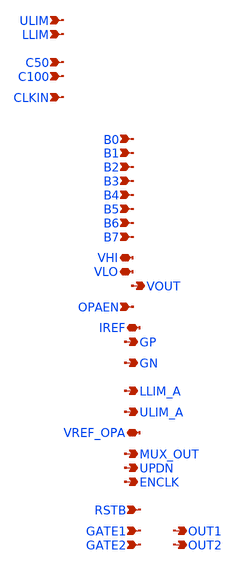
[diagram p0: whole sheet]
** sch_path: xschem/twg_PEX.sch
**.subckt twg_PEX ULIM C50 C100 CLKIN LLIM VHI VLO B0 B1 B2 B3 B4 B5 B6 B7 VOUT OPAEN IREF GP GN
*+ LLIM_A ULIM_A VREF_OPA MUX_OUT UPDN ENCLK RSTB GATE1 GATE2 OUT1 OUT2
*.ipin ULIM
*.ipin C50
*.ipin C100
*.ipin CLKIN
*.ipin LLIM
*.iopin VHI
*.iopin VLO
*.ipin B0
*.ipin B1
*.ipin B2
*.ipin B3
*.ipin B4
*.ipin B5
*.ipin B6
*.ipin B7
*.opin VOUT
*.ipin OPAEN
*.iopin IREF
*.opin GP
*.opin GN
*.opin LLIM_A
*.opin ULIM_A
*.iopin VREF_OPA
*.opin MUX_OUT
*.opin UPDN
*.opin ENCLK
*.ipin RSTB
*.ipin GATE1
*.ipin GATE2
*.opin OUT1
*.opin OUT2
**** begin user architecture code

* NGSPICE file created from twg_top_test.ext - technology: sky130A

.subckt sky130_fd_sc_hs__diode_2 DIODE VGND VPB VPWR VNB
D0 VNB DIODE sky130_fd_pr__diode_pw2nd_05v5 pj=3.24e+06 area=6.417e+11
.ends

.subckt sky130_fd_sc_hs__decap_8 VGND VPWR VNB VPB
X0 VPWR VGND VPWR VPB sky130_fd_pr__pfet_01v8 ad=8.35e+11p pd=7.67e+06u as=0p ps=0u w=1e+06u
+ l=1e+06u
X1 VPWR VGND VPWR VPB sky130_fd_pr__pfet_01v8 ad=0p pd=0u as=0p ps=0u w=1e+06u l=1e+06u
X2 VGND VPWR VGND VNB sky130_fd_pr__nfet_01v8_lvt ad=3.465e+11p pd=4.17e+06u as=0p ps=0u w=420000u
+ l=1e+06u
X3 VGND VPWR VGND VNB sky130_fd_pr__nfet_01v8_lvt ad=0p pd=0u as=0p ps=0u w=420000u l=1e+06u
.ends

.subckt tcap_50f C S VLO
X0 a_173_157# C sky130_fd_pr__cap_mim_m3_2 l=1.6e+06u w=7.85e+06u
X1 a_173_157# S VLO VLO sky130_fd_pr__nfet_01v8 ad=5.8e+11p pd=4.58e+06u as=5.8e+11p ps=4.58e+06u
+ w=2e+06u l=150000u
X2 C a_173_157# sky130_fd_pr__cap_mim_m3_1 l=1.6e+06u w=7.85e+06u
.ends

.subckt sky130_fd_sc_hs__mux2_1 A0 A1 S VGND VPWR X VNB VPB
X0 VGND a_27_112# a_443_74# VNB sky130_fd_pr__nfet_01v8_lvt ad=7.0725e+11p pd=4.91e+06u
+ as=5.994e+11p ps=3.1e+06u w=740000u l=150000u
X1 VPWR S a_27_112# VPB sky130_fd_pr__pfet_01v8 ad=8.82e+11p pd=5.95e+06u as=2.478e+11p ps=2.27e+06u
+ w=840000u l=150000u
X2 X a_304_74# VPWR VPB sky130_fd_pr__pfet_01v8 ad=3.304e+11p pd=2.83e+06u as=0p ps=0u w=1.12e+06u
+ l=150000u
X3 VPWR a_27_112# a_524_368# VPB sky130_fd_pr__pfet_01v8 ad=0p pd=0u as=4.2e+11p ps=2.84e+06u
+ w=1e+06u l=150000u
X4 a_304_74# A1 a_226_74# VNB sky130_fd_pr__nfet_01v8_lvt ad=4.033e+11p pd=2.57e+06u as=1.776e+11p
+ ps=1.96e+06u w=740000u l=150000u
X5 X a_304_74# VGND VNB sky130_fd_pr__nfet_01v8_lvt ad=2.109e+11p pd=2.05e+06u as=0p ps=0u w=740000u
+ l=150000u
X6 a_223_368# S VPWR VPB sky130_fd_pr__pfet_01v8 ad=8.15e+11p pd=3.63e+06u as=0p ps=0u w=1e+06u
+ l=150000u
X7 a_304_74# A0 a_223_368# VPB sky130_fd_pr__pfet_01v8 ad=3.9e+11p pd=2.78e+06u as=0p ps=0u w=1e+06u
+ l=150000u
X8 a_443_74# A0 a_304_74# VNB sky130_fd_pr__nfet_01v8_lvt ad=0p pd=0u as=0p ps=0u w=740000u
+ l=150000u
X9 a_524_368# A1 a_304_74# VPB sky130_fd_pr__pfet_01v8 ad=0p pd=0u as=0p ps=0u w=1e+06u l=150000u
X10 a_226_74# S VGND VNB sky130_fd_pr__nfet_01v8_lvt ad=0p pd=0u as=0p ps=0u w=740000u l=150000u
X11 VGND S a_27_112# VNB sky130_fd_pr__nfet_01v8_lvt ad=0p pd=0u as=1.5675e+11p ps=1.67e+06u
+ w=550000u l=150000u
.ends

.subckt sky130_fd_sc_hs__decap_4 VGND VPWR VNB VPB
X0 VPWR VGND VPWR VPB sky130_fd_pr__pfet_01v8 ad=5.6e+11p pd=5.12e+06u as=0p ps=0u w=1e+06u l=1e+06u
X1 VGND VPWR VGND VNB sky130_fd_pr__nfet_01v8_lvt ad=2.31e+11p pd=2.78e+06u as=0p ps=0u w=420000u
+ l=1e+06u
.ends

.subckt tcap_100f C S VLO
X0 a_173_157# C sky130_fd_pr__cap_mim_m3_2 l=1.6e+06u w=1.57e+07u
X1 a_173_157# S VLO VLO sky130_fd_pr__nfet_01v8 ad=5.8e+11p pd=4.58e+06u as=5.8e+11p ps=4.58e+06u
+ w=2e+06u l=150000u
X2 C a_173_157# sky130_fd_pr__cap_mim_m3_1 l=1.6e+06u w=1.57e+07u
.ends

.subckt sky130_fd_sc_hs__sdfbbn_2 CLK_N D RESET_B SCD SCE SET_B VGND VPWR Q Q_N VNB  VPB
X0 a_1997_82# a_868_368# a_1986_424# VPB sky130_fd_pr__pfet_01v8 ad=2.856e+11p pd=2.45e+06u
+ as=2.016e+11p ps=2.16e+06u w=840000u l=150000u
X1 a_1185_125# a_1007_366# VGND VNB sky130_fd_pr__nfet_01v8_lvt ad=8.82e+10p pd=1.26e+06u
+ as=2.86405e+12p ps=2.37e+07u w=420000u l=150000u
X2 a_2452_74# SET_B VGND VNB sky130_fd_pr__nfet_01v8_lvt ad=5.7435e+11p pd=4.64e+06u as=0p ps=0u
+ w=740000u l=150000u
X3 a_1070_464# a_1007_366# VPWR VPB sky130_fd_pr__pfet_01v8 ad=1.134e+11p pd=1.38e+06u
+ as=4.12873e+12p ps=3.022e+07u w=420000u l=150000u
X4 a_363_119# D a_197_119# VNB sky130_fd_pr__nfet_01v8_lvt ad=1.008e+11p pd=1.32e+06u as=4.347e+11p
+ ps=3.75e+06u w=420000u l=150000u
X5 VGND a_2216_410# Q_N VNB sky130_fd_pr__nfet_01v8_lvt ad=0p pd=0u as=2.072e+11p ps=2.04e+06u
+ w=740000u l=150000u
X6 VGND a_2216_410# a_3272_94# VNB sky130_fd_pr__nfet_01v8_lvt ad=0p pd=0u as=1.824e+11p
+ ps=1.85e+06u w=640000u l=150000u
X7 a_119_119# SCD VGND VNB sky130_fd_pr__nfet_01v8_lvt ad=1.008e+11p pd=1.32e+06u as=0p ps=0u
+ w=420000u l=150000u
X8 VGND SET_B a_1473_73# VNB sky130_fd_pr__nfet_01v8_lvt ad=0p pd=0u as=6.0335e+11p ps=4.55e+06u
+ w=550000u l=150000u
X9 a_2247_82# a_868_368# a_1997_82# VNB sky130_fd_pr__nfet_01v8_lvt ad=1.008e+11p pd=1.32e+06u
+ as=4.945e+11p ps=3.3e+06u w=420000u l=150000u
X10 VGND CLK_N a_688_98# VNB sky130_fd_pr__nfet_01v8_lvt ad=0p pd=0u as=2.109e+11p ps=2.05e+06u
+ w=740000u l=150000u
X11 a_868_368# a_688_98# VGND VNB sky130_fd_pr__nfet_01v8_lvt ad=2.109e+11p pd=2.05e+06u as=0p ps=0u
+ w=740000u l=150000u
X12 VPWR a_3272_94# Q VPB sky130_fd_pr__pfet_01v8 ad=0p pd=0u as=3.36e+11p ps=2.84e+06u w=1.12e+06u
+ l=150000u
X13 a_2452_74# a_1997_82# a_2216_410# VNB sky130_fd_pr__nfet_01v8_lvt ad=0p pd=0u as=2.072e+11p
+ ps=2.04e+06u w=740000u l=150000u
X14 VPWR SCD a_27_464# VPB sky130_fd_pr__pfet_01v8 ad=0p pd=0u as=3.776e+11p ps=3.74e+06u w=640000u
+ l=150000u
X15 Q a_3272_94# VPWR VPB sky130_fd_pr__pfet_01v8 ad=0p pd=0u as=0p ps=0u w=1.12e+06u l=150000u
X16 a_1986_424# a_1007_366# VPWR VPB sky130_fd_pr__pfet_01v8 ad=0p pd=0u as=0p ps=0u w=840000u
+ l=150000u
X17 VPWR a_2216_410# a_2171_508# VPB sky130_fd_pr__pfet_01v8 ad=0p pd=0u as=1.008e+11p ps=1.32e+06u
+ w=420000u l=150000u
X18 a_2216_410# a_1997_82# a_2556_392# VPB sky130_fd_pr__pfet_01v8 ad=5.9e+11p pd=5.18e+06u
+ as=2.7e+11p ps=2.54e+06u w=1e+06u l=150000u
X19 a_341_410# SCE VPWR VPB sky130_fd_pr__pfet_01v8 ad=1.888e+11p pd=1.87e+06u as=0p ps=0u w=640000u
+ l=150000u
X20 a_1007_366# a_1154_464# a_1473_73# VNB sky130_fd_pr__nfet_01v8_lvt ad=1.54e+11p pd=1.66e+06u
+ as=0p ps=0u w=550000u l=150000u
X21 VPWR SET_B a_2216_410# VPB sky130_fd_pr__pfet_01v8 ad=0p pd=0u as=0p ps=0u w=1e+06u l=150000u
X22 VGND a_3272_94# Q VNB sky130_fd_pr__nfet_01v8_lvt ad=0p pd=0u as=2.072e+11p ps=2.04e+06u
+ w=740000u l=150000u
X23 VPWR a_1643_257# a_1592_424# VPB sky130_fd_pr__pfet_01v8 ad=0p pd=0u as=2.268e+11p ps=2.22e+06u
+ w=840000u l=150000u
X24 a_2171_508# a_688_98# a_1997_82# VPB sky130_fd_pr__pfet_01v8 ad=0p pd=0u as=0p ps=0u w=420000u
+ l=150000u
X25 a_1997_82# a_688_98# a_1902_125# VNB sky130_fd_pr__nfet_01v8_lvt ad=0p pd=0u as=2.16375e+11p
+ ps=2.18e+06u w=550000u l=150000u
X26 a_2556_392# a_1643_257# VPWR VPB sky130_fd_pr__pfet_01v8 ad=0p pd=0u as=0p ps=0u w=1e+06u
+ l=150000u
X27 a_1592_424# a_1154_464# a_1007_366# VPB sky130_fd_pr__pfet_01v8 ad=0p pd=0u as=9.954e+11p
+ ps=5.73e+06u w=840000u l=150000u
X28 a_1007_366# SET_B VPWR VPB sky130_fd_pr__pfet_01v8 ad=0p pd=0u as=0p ps=0u w=840000u l=150000u
X29 VPWR RESET_B a_1643_257# VPB sky130_fd_pr__pfet_01v8 ad=0p pd=0u as=1.888e+11p ps=1.87e+06u
+ w=640000u l=150000u
X30 VPWR a_2216_410# Q_N VPB sky130_fd_pr__pfet_01v8 ad=0p pd=0u as=3.36e+11p ps=2.84e+06u
+ w=1.12e+06u l=150000u
X31 a_2216_410# a_1643_257# a_2452_74# VNB sky130_fd_pr__nfet_01v8_lvt ad=0p pd=0u as=0p ps=0u
+ w=740000u l=150000u
X32 a_197_119# SCE a_119_119# VNB sky130_fd_pr__nfet_01v8_lvt ad=0p pd=0u as=0p ps=0u w=420000u
+ l=150000u
X33 Q_N a_2216_410# VPWR VPB sky130_fd_pr__pfet_01v8 ad=0p pd=0u as=0p ps=0u w=1.12e+06u l=150000u
X34 VGND a_2216_410# a_2247_82# VNB sky130_fd_pr__nfet_01v8_lvt ad=0p pd=0u as=0p ps=0u w=420000u
+ l=150000u
X35 a_27_464# a_341_410# a_197_119# VPB sky130_fd_pr__pfet_01v8 ad=0p pd=0u as=4.128e+11p
+ ps=3.85e+06u w=640000u l=150000u
X36 a_1473_73# a_1643_257# a_1007_366# VNB sky130_fd_pr__nfet_01v8_lvt ad=0p pd=0u as=0p ps=0u
+ w=550000u l=150000u
X37 a_197_119# D a_206_464# VPB sky130_fd_pr__pfet_01v8 ad=0p pd=0u as=1.536e+11p ps=1.76e+06u
+ w=640000u l=150000u
X38 a_1154_464# a_688_98# a_1185_125# VNB sky130_fd_pr__nfet_01v8_lvt ad=1.281e+11p pd=1.45e+06u
+ as=0p ps=0u w=420000u l=150000u
X39 a_1902_125# a_1007_366# VGND VNB sky130_fd_pr__nfet_01v8_lvt ad=0p pd=0u as=0p ps=0u w=550000u
+ l=150000u
X40 Q a_3272_94# VGND VNB sky130_fd_pr__nfet_01v8_lvt ad=0p pd=0u as=0p ps=0u w=740000u l=150000u
X41 a_197_119# a_688_98# a_1154_464# VPB sky130_fd_pr__pfet_01v8 ad=0p pd=0u as=2.266e+11p
+ ps=2.05e+06u w=640000u l=150000u
X42 VPWR a_2216_410# a_3272_94# VPB sky130_fd_pr__pfet_01v8 ad=0p pd=0u as=2.9e+11p ps=2.58e+06u
+ w=1e+06u l=150000u
X43 VGND RESET_B a_1643_257# VNB sky130_fd_pr__nfet_01v8_lvt ad=0p pd=0u as=1.176e+11p ps=1.4e+06u
+ w=420000u l=150000u
X44 a_868_368# a_688_98# VPWR VPB sky130_fd_pr__pfet_01v8 ad=3.304e+11p pd=2.83e+06u as=0p ps=0u
+ w=1.12e+06u l=150000u
X45 a_197_119# a_868_368# a_1154_464# VNB sky130_fd_pr__nfet_01v8_lvt ad=0p pd=0u as=0p ps=0u
+ w=420000u l=150000u
X46 a_206_464# SCE VPWR VPB sky130_fd_pr__pfet_01v8 ad=0p pd=0u as=0p ps=0u w=640000u l=150000u
X47 VPWR CLK_N a_688_98# VPB sky130_fd_pr__pfet_01v8 ad=0p pd=0u as=3.304e+11p ps=2.83e+06u
+ w=1.12e+06u l=150000u
X48 a_1154_464# a_868_368# a_1070_464# VPB sky130_fd_pr__pfet_01v8 ad=0p pd=0u as=0p ps=0u w=420000u
+ l=150000u
X49 VGND a_341_410# a_363_119# VNB sky130_fd_pr__nfet_01v8_lvt ad=0p pd=0u as=0p ps=0u w=420000u
+ l=150000u
X50 a_341_410# SCE VGND VNB sky130_fd_pr__nfet_01v8_lvt ad=1.197e+11p pd=1.41e+06u as=0p ps=0u
+ w=420000u l=150000u
X51 Q_N a_2216_410# VGND VNB sky130_fd_pr__nfet_01v8_lvt ad=0p pd=0u as=0p ps=0u w=740000u l=150000u
.ends

.subckt sky130_fd_sc_hs__inv_1 A VGND VPWR Y VNB VPB
X0 Y A VPWR VPB sky130_fd_pr__pfet_01v8 ad=3.304e+11p pd=2.83e+06u as=3.864e+11p ps=2.93e+06u
+ w=1.12e+06u l=150000u
X1 Y A VGND VNB sky130_fd_pr__nfet_01v8_lvt ad=2.109e+11p pd=2.05e+06u as=2.627e+11p ps=2.19e+06u
+ w=740000u l=150000u
.ends

.subckt sky130_fd_sc_hs__nand2_1 A B VGND VPWR Y VNB VPB
X0 a_117_74# B VGND VNB sky130_fd_pr__nfet_01v8_lvt ad=1.776e+11p pd=1.96e+06u as=2.109e+11p
+ ps=2.05e+06u w=740000u l=150000u
X1 VPWR A Y VPB sky130_fd_pr__pfet_01v8 ad=6.384e+11p pd=5.62e+06u as=3.36e+11p ps=2.84e+06u
+ w=1.12e+06u l=150000u
X2 Y A a_117_74# VNB sky130_fd_pr__nfet_01v8_lvt ad=2.109e+11p pd=2.05e+06u as=0p ps=0u w=740000u
+ l=150000u
X3 Y B VPWR VPB sky130_fd_pr__pfet_01v8 ad=0p pd=0u as=0p ps=0u w=1.12e+06u l=150000u
.ends

.subckt sky130_fd_pr__res_xhigh_po_1p41_GKKP9B a_n141_n482# a_n141_50# VSUBS
X0 a_n141_n482# a_n141_50# VSUBS sky130_fd_pr__res_xhigh_po_1p41 l=500000u
.ends

.subckt twcon_tdly C A Y sky130_fd_sc_hs__inv_1_0/VGND VSUBS sky130_fd_sc_hs__inv_1_0/VPWR
+  sky130_fd_sc_hs__inv_1_0/VPB
Xsky130_fd_sc_hs__inv_1_0 A sky130_fd_sc_hs__inv_1_0/VGND sky130_fd_sc_hs__inv_1_0/VPWR
+  sky130_fd_sc_hs__inv_1_0/Y VSUBS sky130_fd_sc_hs__inv_1_0/VPB sky130_fd_sc_hs__inv_1
Xsky130_fd_sc_hs__nand2_1_2 A C sky130_fd_sc_hs__inv_1_0/VGND sky130_fd_sc_hs__inv_1_0/VPWR  Y VSUBS
+ sky130_fd_sc_hs__inv_1_0/VPB sky130_fd_sc_hs__nand2_1
Xsky130_fd_pr__res_xhigh_po_1p41_GKKP9B_0 sky130_fd_sc_hs__inv_1_0/Y C VSUBS
+ sky130_fd_pr__res_xhigh_po_1p41_GKKP9B
.ends

.subckt sky130_fd_sc_hs__nand2_4 A B VGND VPWR Y VNB VPB
X0 Y A a_27_74# VNB sky130_fd_pr__nfet_01v8_lvt ad=5.365e+11p pd=4.41e+06u as=1.1581e+12p
+ ps=1.053e+07u w=740000u l=150000u
X1 Y B VPWR VPB sky130_fd_pr__pfet_01v8 ad=2.7496e+12p pd=9.39e+06u as=1.1144e+12p ps=8.71e+06u
+ w=1.12e+06u l=150000u
X2 VPWR A Y VPB sky130_fd_pr__pfet_01v8 ad=0p pd=0u as=0p ps=0u w=1.12e+06u l=150000u
X3 Y A a_27_74# VNB sky130_fd_pr__nfet_01v8_lvt ad=0p pd=0u as=0p ps=0u w=740000u l=150000u
X4 Y A VPWR VPB sky130_fd_pr__pfet_01v8 ad=0p pd=0u as=0p ps=0u w=1.12e+06u l=150000u
X5 VGND B a_27_74# VNB sky130_fd_pr__nfet_01v8_lvt ad=4.144e+11p pd=4.08e+06u as=0p ps=0u w=740000u
+ l=150000u
X6 a_27_74# A Y VNB sky130_fd_pr__nfet_01v8_lvt ad=0p pd=0u as=0p ps=0u w=740000u l=150000u
X7 VPWR B Y VPB sky130_fd_pr__pfet_01v8 ad=0p pd=0u as=0p ps=0u w=1.12e+06u l=150000u
X8 a_27_74# B VGND VNB sky130_fd_pr__nfet_01v8_lvt ad=0p pd=0u as=0p ps=0u w=740000u l=150000u
X9 a_27_74# A Y VNB sky130_fd_pr__nfet_01v8_lvt ad=0p pd=0u as=0p ps=0u w=740000u l=150000u
X10 a_27_74# B VGND VNB sky130_fd_pr__nfet_01v8_lvt ad=0p pd=0u as=0p ps=0u w=740000u l=150000u
X11 VGND B a_27_74# VNB sky130_fd_pr__nfet_01v8_lvt ad=0p pd=0u as=0p ps=0u w=740000u l=150000u
.ends

.subckt sky130_fd_sc_hs__inv_2 A VGND VPWR Y VNB VPB
X0 Y A VGND VNB sky130_fd_pr__nfet_01v8_lvt ad=2.072e+11p pd=2.04e+06u as=4.218e+11p ps=4.1e+06u
+ w=740000u l=150000u
X1 VPWR A Y VPB sky130_fd_pr__pfet_01v8 ad=6.384e+11p pd=5.62e+06u as=3.36e+11p ps=2.84e+06u
+ w=1.12e+06u l=150000u
X2 VGND A Y VNB sky130_fd_pr__nfet_01v8_lvt ad=0p pd=0u as=0p ps=0u w=740000u l=150000u
X3 Y A VPWR VPB sky130_fd_pr__pfet_01v8 ad=0p pd=0u as=0p ps=0u w=1.12e+06u l=150000u
.ends

.subckt sky130_fd_sc_hs__and2_4 A B VGND VPWR X VNB VPB
X0 X a_83_269# VPWR VPB sky130_fd_pr__pfet_01v8 ad=6.944e+11p pd=5.72e+06u as=1.58705e+12p
+ ps=1.328e+07u w=1.12e+06u l=150000u
X1 a_83_269# B VPWR VPB sky130_fd_pr__pfet_01v8 ad=5.25e+11p pd=4.61e+06u as=0p ps=0u w=840000u
+ l=150000u
X2 a_83_269# A a_504_119# VNB sky130_fd_pr__nfet_01v8_lvt ad=2.08e+11p pd=1.93e+06u as=3.872e+11p
+ ps=3.77e+06u w=640000u l=150000u
X3 VPWR a_83_269# X VPB sky130_fd_pr__pfet_01v8 ad=0p pd=0u as=0p ps=0u w=1.12e+06u l=150000u
X4 VGND a_83_269# X VNB sky130_fd_pr__nfet_01v8_lvt ad=8.594e+11p pd=8.14e+06u as=5.254e+11p
+ ps=4.38e+06u w=740000u l=150000u
X5 X a_83_269# VGND VNB sky130_fd_pr__nfet_01v8_lvt ad=0p pd=0u as=0p ps=0u w=740000u l=150000u
X6 X a_83_269# VPWR VPB sky130_fd_pr__pfet_01v8 ad=0p pd=0u as=0p ps=0u w=1.12e+06u l=150000u
X7 VPWR a_83_269# X VPB sky130_fd_pr__pfet_01v8 ad=0p pd=0u as=0p ps=0u w=1.12e+06u l=150000u
X8 VPWR B a_83_269# VPB sky130_fd_pr__pfet_01v8 ad=0p pd=0u as=0p ps=0u w=840000u l=150000u
X9 a_83_269# A VPWR VPB sky130_fd_pr__pfet_01v8 ad=0p pd=0u as=0p ps=0u w=840000u l=150000u
X10 VGND a_83_269# X VNB sky130_fd_pr__nfet_01v8_lvt ad=0p pd=0u as=0p ps=0u w=740000u l=150000u
X11 VPWR A a_83_269# VPB sky130_fd_pr__pfet_01v8 ad=0p pd=0u as=0p ps=0u w=840000u l=150000u
X12 VGND B a_504_119# VNB sky130_fd_pr__nfet_01v8_lvt ad=0p pd=0u as=0p ps=0u w=640000u l=150000u
X13 a_504_119# A a_83_269# VNB sky130_fd_pr__nfet_01v8_lvt ad=0p pd=0u as=0p ps=0u w=640000u
+ l=150000u
X14 X a_83_269# VGND VNB sky130_fd_pr__nfet_01v8_lvt ad=0p pd=0u as=0p ps=0u w=740000u l=150000u
X15 a_504_119# B VGND VNB sky130_fd_pr__nfet_01v8_lvt ad=0p pd=0u as=0p ps=0u w=640000u l=150000u
.ends

.subckt twcon UPDN A0 A1 RSTB C100 C50 MUX_OUT ENCLK GN GP CLKIN VHI VLO
Xsky130_fd_sc_hs__decap_8_0 VLO VHI VLO VHI sky130_fd_sc_hs__decap_8
Xtcap_50f_0 tcap_50f_0/C C100 VLO tcap_50f
Xsky130_fd_sc_hs__decap_8_2 VLO VHI VLO VHI sky130_fd_sc_hs__decap_8
Xsky130_fd_sc_hs__decap_8_3 VLO VHI VLO VHI sky130_fd_sc_hs__decap_8
Xtcap_50f_3 tcap_50f_3/C C100 VLO tcap_50f
Xsky130_fd_sc_hs__decap_8_4 VLO VHI VLO VHI sky130_fd_sc_hs__decap_8
Xtcap_50f_2 tcap_50f_2/C C50 VLO tcap_50f
Xsky130_fd_sc_hs__mux2_1_1 twcon_tdly_1/Y twcon_tdly_2/Y sky130_fd_sc_hs__mux2_1_1/S  VLO VHI
+ MUX_OUT VLO VHI sky130_fd_sc_hs__mux2_1
Xsky130_fd_sc_hs__decap_8_6 VLO VHI VLO VHI sky130_fd_sc_hs__decap_8
Xsky130_fd_sc_hs__decap_4_0 VLO VHI VLO VHI sky130_fd_sc_hs__decap_4
Xsky130_fd_sc_hs__decap_8_7 VLO VHI VLO VHI sky130_fd_sc_hs__decap_8
Xtcap_100f_0 tcap_50f_0/C C50 VLO tcap_100f
Xtcap_100f_2 tcap_50f_2/C C100 VLO tcap_100f
Xtcap_100f_3 tcap_50f_3/C C50 VLO tcap_100f
Xsky130_fd_sc_hs__sdfbbn_2_0 ENCLK VHI MUX_OUT VLO VLO VHI VLO VHI sky130_fd_sc_hs__and2_4_0/B
+  sky130_fd_sc_hs__sdfbbn_2_0/Q_N VLO VHI sky130_fd_sc_hs__sdfbbn_2
Xsky130_fd_sc_hs__sdfbbn_2_1 twcon_tdly_0/Y sky130_fd_sc_hs__mux2_1_1/S RSTB VLO VLO  VHI VLO VHI
+ UPDN sky130_fd_sc_hs__mux2_1_1/S VLO VHI sky130_fd_sc_hs__sdfbbn_2
Xtwcon_tdly_0 tcap_50f_2/C CLKIN twcon_tdly_0/Y VLO VLO VHI VHI twcon_tdly
Xtwcon_tdly_1 tcap_50f_0/C A0 twcon_tdly_1/Y VLO VLO VHI VHI twcon_tdly
Xtwcon_tdly_2 tcap_50f_3/C A1 twcon_tdly_2/Y VLO VLO VHI VHI twcon_tdly
Xsky130_fd_sc_hs__nand2_4_3 sky130_fd_sc_hs__and2_4_0/B UPDN VLO VHI GP VLO VHI
+ sky130_fd_sc_hs__nand2_4
Xsky130_fd_sc_hs__inv_2_1 CLKIN VLO VHI ENCLK VLO VHI sky130_fd_sc_hs__inv_2
Xsky130_fd_sc_hs__and2_4_0 sky130_fd_sc_hs__mux2_1_1/S sky130_fd_sc_hs__and2_4_0/B  VLO VHI GN VLO
+ VHI sky130_fd_sc_hs__and2_4
.ends

.subckt imirror2 OUT VLO VHI IN
X0 VHI a_4493_207# a_4493_207# VHI sky130_fd_pr__pfet_01v8 ad=2.9e+12p pd=2.058e+07u as=2.9e+12p
+ ps=2.058e+07u w=1e+07u l=2e+06u
X1 a_4493_207# VLO VLO VLO sky130_fd_pr__nfet_01v8 ad=1.45e+12p pd=1.058e+07u as=4.35e+12p
+ ps=3.174e+07u w=5e+06u l=2e+06u
X2 VLO VLO OUT VLO sky130_fd_pr__nfet_01v8 ad=0p pd=0u as=1.45e+12p ps=1.058e+07u w=5e+06u l=2e+06u
X3 a_5868_1637# a_5468_1540# OUT VHI sky130_fd_pr__pfet_01v8 ad=2.9e+12p pd=2.058e+07u as=2.9e+12p
+ ps=2.058e+07u w=1e+07u l=2e+06u
X4 OUT OUT VLO VLO sky130_fd_pr__nfet_01v8 ad=0p pd=0u as=0p ps=0u w=5e+06u l=2e+06u
X5 VLO IN a_4493_207# VLO sky130_fd_pr__nfet_01v8 ad=0p pd=0u as=0p ps=0u w=5e+06u l=2e+06u
X6 a_4493_207# a_4094_1540# a_4036_1637# VHI sky130_fd_pr__pfet_01v8 ad=0p pd=0u as=2.9e+12p
+ ps=2.058e+07u w=1e+07u l=2e+06u
X7 OUT a_4493_207# VHI VHI sky130_fd_pr__pfet_01v8 ad=0p pd=0u as=0p ps=0u w=1e+07u l=2e+06u
.ends

.subckt gated_iref_fix imirror2_0/VHI SBAR VSUB a_1712_150# S imirror2_0/IN
Ximirror2_0 imirror2_0/OUT VSUB imirror2_0/VHI imirror2_0/IN imirror2
X0 imirror2_0/OUT a_1444_106# VSUB sky130_fd_pr__res_xhigh_po w=350000u l=1.49e+06u
X1 VSUB SBAR a_1712_150# VSUB sky130_fd_pr__nfet_01v8 ad=5.95e+12p pd=4.302e+07u as=1.65e+12p
+ ps=1.132e+07u w=2.5e+06u l=150000u
X2 VSUB a_1712_150# sky130_fd_pr__cap_mim_m3_1 l=6.2e+06u w=2.76e+07u
X3 a_1712_150# VSUB sky130_fd_pr__cap_mim_m3_2 l=6.2e+06u w=2.76e+07u
X4 a_1712_150# S a_1444_106# VSUB sky130_fd_pr__nfet_01v8 ad=0p pd=0u as=1.6e+12p ps=1.128e+07u
+ w=2.5e+06u l=150000u
X5 VSUB VSUB a_1444_106# VSUB sky130_fd_pr__nfet_01v8 ad=0p pd=0u as=0p ps=0u w=2.5e+06u l=150000u
X6 a_1712_150# SBAR VSUB VSUB sky130_fd_pr__nfet_01v8 ad=0p pd=0u as=0p ps=0u w=2.5e+06u l=150000u
X7 a_1444_106# S a_1712_150# VSUB sky130_fd_pr__nfet_01v8 ad=0p pd=0u as=0p ps=0u w=2.5e+06u
+ l=150000u
.ends

.subckt sky130_fd_pr__res_high_po_0p69_G8QCSG a_48_n518# a_n186_n518# a_n316_n648#
X0 a_n186_n518# a_48_n518# a_n316_n648# sky130_fd_pr__res_high_po w=690000u l=5.83e+06u
.ends

.subckt cmota_gb_rp VREF VIP VIN VLO VOP VHI
Xsky130_fd_pr__res_high_po_0p69_G8QCSG_0 li_5300_n960# VMN VLO sky130_fd_pr__res_high_po_0p69_G8QCSG
X0 VHI DN VMN VHI sky130_fd_pr__pfet_01v8 ad=4.93e+13p pd=3.4986e+08u as=1.16e+13p ps=8.232e+07u
+ w=1e+07u l=300000u
X1 VHI DN DN VHI sky130_fd_pr__pfet_01v8 ad=0p pd=0u as=8.7e+12p ps=6.174e+07u w=1e+07u l=300000u
X2 VHI DP VOP VHI sky130_fd_pr__pfet_01v8 ad=0p pd=0u as=1.16e+13p ps=8.232e+07u w=1e+07u l=300000u
X3 DN VIN COM VLO sky130_fd_pr__nfet_01v8_lvt ad=3.3e+12p pd=2.264e+07u as=1.3225e+13p ps=9.21e+07u
+ w=2.5e+06u l=150000u
X4 COM VIN DN VLO sky130_fd_pr__nfet_01v8_lvt ad=0p pd=0u as=0p ps=0u w=2.5e+06u l=150000u
X5 DP VIP COM VLO sky130_fd_pr__nfet_01v8_lvt ad=3.3e+12p pd=2.264e+07u as=0p ps=0u w=2.5e+06u
+ l=150000u
X6 VMN DN VHI VHI sky130_fd_pr__pfet_01v8 ad=0p pd=0u as=0p ps=0u w=1e+07u l=300000u
X7 VMN DN VHI VHI sky130_fd_pr__pfet_01v8 ad=0p pd=0u as=0p ps=0u w=1e+07u l=300000u
X8 VHI VHI VOP VHI sky130_fd_pr__pfet_01v8 ad=0p pd=0u as=0p ps=0u w=1e+07u l=300000u
X9 a_2925_285# DN VHI VHI sky130_fd_pr__pfet_01v8 ad=2.9e+12p pd=2.058e+07u as=0p ps=0u w=1e+07u
+ l=300000u
X10 DP VIP COM VLO sky130_fd_pr__nfet_01v8_lvt ad=0p pd=0u as=0p ps=0u w=2.5e+06u l=150000u
X11 li_5300_n960# VOP sky130_fd_pr__cap_mim_m3_2 l=1.32e+07u w=3.7e+06u
X12 VOP DP VHI VHI sky130_fd_pr__pfet_01v8 ad=0p pd=0u as=0p ps=0u w=1e+07u l=300000u
X13 VOP DP VHI VHI sky130_fd_pr__pfet_01v8 ad=0p pd=0u as=0p ps=0u w=1e+07u l=300000u
X14 VOP DP VHI VHI sky130_fd_pr__pfet_01v8 ad=0p pd=0u as=0p ps=0u w=1e+07u l=300000u
X15 COM VLO VLO VLO sky130_fd_pr__nfet_01v8_lvt ad=0p pd=0u as=3.8e+13p ps=2.69525e+08u w=2.5e+06u
+ l=150000u
X16 VLO VMN VOP VLO sky130_fd_pr__nfet_01v8 ad=0p pd=0u as=5.8e+12p ps=4.116e+07u w=1e+07u l=300000u
X17 VHI DN VMN VHI sky130_fd_pr__pfet_01v8 ad=0p pd=0u as=0p ps=0u w=1e+07u l=300000u
X18 VLO VLO VLO VLO sky130_fd_pr__nfet_01v8 ad=0p pd=0u as=0p ps=0u w=1e+07u l=300000u
X19 VHI DN DP VHI sky130_fd_pr__pfet_01v8 ad=0p pd=0u as=8.7e+12p ps=6.174e+07u w=1e+07u l=300000u
X20 VHI DP DP VHI sky130_fd_pr__pfet_01v8 ad=0p pd=0u as=0p ps=0u w=1e+07u l=300000u
X21 COM VIP DP VLO sky130_fd_pr__nfet_01v8_lvt ad=0p pd=0u as=0p ps=0u w=2.5e+06u l=150000u
X22 VLO VREF COM VLO sky130_fd_pr__nfet_01v8 ad=0p pd=0u as=0p ps=0u w=1e+07u l=2e+06u
X23 VMN VHI VHI VHI sky130_fd_pr__pfet_01v8 ad=0p pd=0u as=0p ps=0u w=1e+07u l=300000u
X24 DN DN VHI VHI sky130_fd_pr__pfet_01v8 ad=0p pd=0u as=0p ps=0u w=1e+07u l=300000u
X25 VHI DP VOP VHI sky130_fd_pr__pfet_01v8 ad=0p pd=0u as=0p ps=0u w=1e+07u l=300000u
X26 VLO VLO VLO VLO sky130_fd_pr__nfet_01v8_lvt ad=0p pd=0u as=0p ps=0u w=2.5e+06u l=150000u
X27 VLO VREF COM VLO sky130_fd_pr__nfet_01v8 ad=0p pd=0u as=0p ps=0u w=1e+07u l=2e+06u
X28 COM VIN DN VLO sky130_fd_pr__nfet_01v8_lvt ad=0p pd=0u as=0p ps=0u w=2.5e+06u l=150000u
X29 DN DN VHI VHI sky130_fd_pr__pfet_01v8 ad=0p pd=0u as=0p ps=0u w=1e+07u l=300000u
X30 DP DN VHI VHI sky130_fd_pr__pfet_01v8 ad=0p pd=0u as=0p ps=0u w=1e+07u l=300000u
X31 DN DP VHI VHI sky130_fd_pr__pfet_01v8 ad=0p pd=0u as=0p ps=0u w=1e+07u l=300000u
X32 DP DP VHI VHI sky130_fd_pr__pfet_01v8 ad=0p pd=0u as=0p ps=0u w=1e+07u l=300000u
X33 DN VIN COM VLO sky130_fd_pr__nfet_01v8_lvt ad=0p pd=0u as=0p ps=0u w=2.5e+06u l=150000u
X34 VLO VLO VLO VLO sky130_fd_pr__nfet_01v8 ad=0p pd=0u as=0p ps=0u w=1e+07u l=300000u
X35 COM VIP DP VLO sky130_fd_pr__nfet_01v8_lvt ad=0p pd=0u as=0p ps=0u w=2.5e+06u l=150000u
X36 VHI DN DN VHI sky130_fd_pr__pfet_01v8 ad=0p pd=0u as=0p ps=0u w=1e+07u l=300000u
X37 VOP DP VHI VHI sky130_fd_pr__pfet_01v8 ad=0p pd=0u as=0p ps=0u w=1e+07u l=300000u
X38 VMN VMN VLO VLO sky130_fd_pr__nfet_01v8 ad=5.8e+12p pd=4.116e+07u as=0p ps=0u w=1e+07u l=300000u
X39 VLO VMN VMN VLO sky130_fd_pr__nfet_01v8 ad=0p pd=0u as=0p ps=0u w=1e+07u l=300000u
X40 VLO VLO VLO VLO sky130_fd_pr__nfet_01v8 ad=0p pd=0u as=0p ps=0u w=1e+07u l=300000u
X41 VOP VMN VLO VLO sky130_fd_pr__nfet_01v8 ad=0p pd=0u as=0p ps=0u w=1e+07u l=300000u
X42 VHI DP DN VHI sky130_fd_pr__pfet_01v8 ad=0p pd=0u as=0p ps=0u w=1e+07u l=300000u
X43 VLO VMN VOP VLO sky130_fd_pr__nfet_01v8 ad=0p pd=0u as=0p ps=0u w=1e+07u l=300000u
X44 VHI DN VMN VHI sky130_fd_pr__pfet_01v8 ad=0p pd=0u as=0p ps=0u w=1e+07u l=300000u
X45 VLO VLO COM VLO sky130_fd_pr__nfet_01v8_lvt ad=0p pd=0u as=0p ps=0u w=2.5e+06u l=150000u
X46 DN VIN COM VLO sky130_fd_pr__nfet_01v8_lvt ad=0p pd=0u as=0p ps=0u w=2.5e+06u l=150000u
X47 VHI DP a_2217_285# VHI sky130_fd_pr__pfet_01v8 ad=0p pd=0u as=2.9e+12p ps=2.058e+07u w=1e+07u
+ l=300000u
X48 VHI DP DP VHI sky130_fd_pr__pfet_01v8 ad=0p pd=0u as=0p ps=0u w=1e+07u l=300000u
X49 VLO VLO VLO VLO sky130_fd_pr__nfet_01v8 ad=0p pd=0u as=0p ps=0u w=1e+07u l=300000u
X50 COM VREF VLO VLO sky130_fd_pr__nfet_01v8 ad=0p pd=0u as=0p ps=0u w=1e+07u l=2e+06u
X51 VLO VLO VLO VLO sky130_fd_pr__nfet_01v8_lvt ad=0p pd=0u as=0p ps=0u w=2.5e+06u l=150000u
X52 COM VIN DN VLO sky130_fd_pr__nfet_01v8_lvt ad=0p pd=0u as=0p ps=0u w=2.5e+06u l=150000u
X53 COM VREF VLO VLO sky130_fd_pr__nfet_01v8 ad=0p pd=0u as=0p ps=0u w=1e+07u l=2e+06u
X54 DP VIP COM VLO sky130_fd_pr__nfet_01v8_lvt ad=0p pd=0u as=0p ps=0u w=2.5e+06u l=150000u
X55 COM VIN DN VLO sky130_fd_pr__nfet_01v8_lvt ad=0p pd=0u as=0p ps=0u w=2.5e+06u l=150000u
X56 VMN DN VHI VHI sky130_fd_pr__pfet_01v8 ad=0p pd=0u as=0p ps=0u w=1e+07u l=300000u
X57 DP DP VHI VHI sky130_fd_pr__pfet_01v8 ad=0p pd=0u as=0p ps=0u w=1e+07u l=300000u
X58 DP VIP COM VLO sky130_fd_pr__nfet_01v8_lvt ad=0p pd=0u as=0p ps=0u w=2.5e+06u l=150000u
X59 a_2217_285# DP VHI VHI sky130_fd_pr__pfet_01v8 ad=0p pd=0u as=0p ps=0u w=1e+07u l=300000u
X60 VMN VMN VLO VLO sky130_fd_pr__nfet_01v8 ad=0p pd=0u as=0p ps=0u w=1e+07u l=300000u
X61 COM VIP DP VLO sky130_fd_pr__nfet_01v8_lvt ad=0p pd=0u as=0p ps=0u w=2.5e+06u l=150000u
X62 VLO VMN VMN VLO sky130_fd_pr__nfet_01v8 ad=0p pd=0u as=0p ps=0u w=1e+07u l=300000u
X63 VOP VMN VLO VLO sky130_fd_pr__nfet_01v8 ad=0p pd=0u as=0p ps=0u w=1e+07u l=300000u
X64 COM VIP DP VLO sky130_fd_pr__nfet_01v8_lvt ad=0p pd=0u as=0p ps=0u w=2.5e+06u l=150000u
X65 VHI DN VMN VHI sky130_fd_pr__pfet_01v8 ad=0p pd=0u as=0p ps=0u w=1e+07u l=300000u
X66 DN VIN COM VLO sky130_fd_pr__nfet_01v8_lvt ad=0p pd=0u as=0p ps=0u w=2.5e+06u l=150000u
X67 VOP li_5300_n960# sky130_fd_pr__cap_mim_m3_1 l=1.32e+07u w=3.7e+06u
X68 VHI DN a_2925_285# VHI sky130_fd_pr__pfet_01v8 ad=0p pd=0u as=0p ps=0u w=1e+07u l=300000u
X69 VHI DP VOP VHI sky130_fd_pr__pfet_01v8 ad=0p pd=0u as=0p ps=0u w=1e+07u l=300000u
.ends

.subckt cmota_gb_rp_gp SBAR VREF VIP VIN VLO S VOP VHI
Xgated_iref_fix_0 VHI SBAR VLO VREF_GATED S VREF gated_iref_fix
Xcmota_gb_rp_0 VREF_GATED VIP VIN VLO VOP VHI cmota_gb_rp
X0 VLO VHI sky130_fd_pr__cap_mim_m3_2 l=3.1e+07u w=1.3e+07u
X1 VHI VLO sky130_fd_pr__cap_mim_m3_1 l=3.1e+07u w=1.3e+07u
.ends

.subckt sky130hd_esd DIODE VPWR VGND
D0 VGND DIODE sky130_fd_pr__diode_pw2nd_05v5 pj=2.64e+06 area=4.347e+11
D1 DIODE VPWR sky130_fd_pr__diode_pd2nw_05v5 pj=3.34e+06 area=6.552e+11
.ends

.subckt tcap_200f C S VLO
X0 a_173_157# C sky130_fd_pr__cap_mim_m3_2 l=1.6e+06u w=3.14e+07u
X1 a_173_157# S VLO VLO sky130_fd_pr__nfet_01v8 ad=5.8e+11p pd=4.58e+06u as=5.8e+11p ps=4.58e+06u
+ w=2e+06u l=150000u
X2 C a_173_157# sky130_fd_pr__cap_mim_m3_1 l=1.6e+06u w=3.14e+07u
.ends

.subckt swcap_array_1 B7 B6 B5 B4 B3 B2 B0 B1 VSUB C
Xtcap_200f_60 C B7 VSUB tcap_200f
Xtcap_200f_50 C B7 VSUB tcap_200f
Xtcap_200f_61 C B7 VSUB tcap_200f
Xtcap_200f_40 C B7 VSUB tcap_200f
Xtcap_200f_51 C B7 VSUB tcap_200f
Xtcap_200f_62 C B7 VSUB tcap_200f
Xtcap_200f_30 C B6 VSUB tcap_200f
Xtcap_200f_41 C B7 VSUB tcap_200f
Xtcap_200f_52 C B7 VSUB tcap_200f
Xtcap_200f_63 C B7 VSUB tcap_200f
Xtcap_50f_0 C B0 VSUB tcap_50f
Xtcap_200f_31 C B6 VSUB tcap_200f
Xtcap_200f_42 C B7 VSUB tcap_200f
Xtcap_200f_20 C B6 VSUB tcap_200f
Xtcap_200f_53 C B7 VSUB tcap_200f
Xtcap_200f_64 C B7 VSUB tcap_200f
Xtcap_200f_33 C B7 VSUB tcap_200f
Xtcap_200f_32 C B6 VSUB tcap_200f
Xtcap_200f_43 C B7 VSUB tcap_200f
Xtcap_200f_44 C B7 VSUB tcap_200f
Xtcap_200f_22 C B6 VSUB tcap_200f
Xtcap_200f_21 C B6 VSUB tcap_200f
Xtcap_200f_54 C B7 VSUB tcap_200f
Xtcap_200f_10 C B5 VSUB tcap_200f
Xtcap_200f_55 C B7 VSUB tcap_200f
Xtcap_200f_11 C B5 VSUB tcap_200f
Xtcap_200f_65 C B7 VSUB tcap_200f
Xtcap_200f_34 C B7 VSUB tcap_200f
Xtcap_200f_23 C B6 VSUB tcap_200f
Xtcap_200f_45 C B7 VSUB tcap_200f
Xtcap_200f_12 C B5 VSUB tcap_200f
Xtcap_200f_56 C B7 VSUB tcap_200f
Xtcap_200f_0 C B5 VSUB tcap_200f
Xtcap_200f_35 C B7 VSUB tcap_200f
Xtcap_200f_24 C B6 VSUB tcap_200f
Xtcap_200f_46 C B7 VSUB tcap_200f
Xtcap_200f_13 C B5 VSUB tcap_200f
Xtcap_200f_57 C B7 VSUB tcap_200f
Xtcap_200f_36 C B7 VSUB tcap_200f
Xtcap_200f_25 C B6 VSUB tcap_200f
Xtcap_200f_47 C B7 VSUB tcap_200f
Xtcap_200f_14 C B5 VSUB tcap_200f
Xtcap_200f_58 C B7 VSUB tcap_200f
Xtcap_200f_37 C B7 VSUB tcap_200f
Xtcap_200f_26 C B6 VSUB tcap_200f
Xtcap_200f_15 C B6 VSUB tcap_200f
Xtcap_200f_48 C B7 VSUB tcap_200f
Xtcap_200f_59 C B7 VSUB tcap_200f
Xtcap_200f_3 C B2 VSUB tcap_200f
Xtcap_200f_38 C B7 VSUB tcap_200f
Xtcap_200f_27 C B6 VSUB tcap_200f
Xtcap_200f_49 C B7 VSUB tcap_200f
Xtcap_200f_16 C B5 VSUB tcap_200f
Xtcap_200f_4 C B3 VSUB tcap_200f
Xtcap_200f_28 C B6 VSUB tcap_200f
Xtcap_200f_39 C B7 VSUB tcap_200f
Xtcap_200f_17 C B5 VSUB tcap_200f
Xtcap_200f_5 C B3 VSUB tcap_200f
Xtcap_200f_29 C B6 VSUB tcap_200f
Xtcap_200f_18 C B6 VSUB tcap_200f
Xtcap_200f_6 C B4 VSUB tcap_200f
Xtcap_200f_19 C B6 VSUB tcap_200f
Xtcap_200f_8 C B4 VSUB tcap_200f
Xtcap_200f_7 C B4 VSUB tcap_200f
Xtcap_200f_9 C B4 VSUB tcap_200f
Xtcap_100f_0 C B1 VSUB tcap_100f
.ends

.subckt isrc IOUT VLO GP VHI GN VREFN
X0 VLO VLO VLO VLO sky130_fd_pr__nfet_01v8 ad=8.7e+12p pd=6.348e+07u as=0p ps=0u w=5e+06u l=2e+06u
X1 VHI GN IN VHI sky130_fd_pr__pfet_01v8 ad=1.45e+13p pd=1.029e+08u as=2.9e+12p ps=2.058e+07u
+ w=1e+07u l=150000u
X2 VHI VHI VREFP VHI sky130_fd_pr__pfet_01v8 ad=0p pd=0u as=2.9e+12p ps=2.058e+07u w=1e+07u l=2e+06u
X3 VLO GP IP VLO sky130_fd_pr__nfet_01v8 ad=0p pd=0u as=1.45e+12p ps=1.058e+07u w=5e+06u l=150000u
X4 VLO VLO a_314_3386# VLO sky130_fd_pr__nfet_01v8 ad=0p pd=0u as=1.45e+12p ps=1.058e+07u w=5e+06u
+ l=2e+06u
X5 a_314_3386# VREFP VLO sky130_fd_pr__res_xhigh_po w=350000u l=5.17e+06u
X6 VHI VHI VHI VHI sky130_fd_pr__pfet_01v8 ad=0p pd=0u as=0p ps=0u w=1e+07u l=2e+06u
X7 VLO VLO VREFN VLO sky130_fd_pr__nfet_01v8 ad=0p pd=0u as=1.45e+12p ps=1.058e+07u w=5e+06u
+ l=2e+06u
X8 IP VREFP VHI VHI sky130_fd_pr__pfet_01v8 ad=5.8e+12p pd=4.116e+07u as=0p ps=0u w=1e+07u l=2e+06u
X9 IN VREFN VLO VLO sky130_fd_pr__nfet_01v8 ad=2.9e+12p pd=2.116e+07u as=0p ps=0u w=5e+06u l=2e+06u
X10 IOUT GP IP VHI sky130_fd_pr__pfet_01v8 ad=2.9e+12p pd=2.058e+07u as=0p ps=0u w=1e+07u l=150000u
X11 VHI VHI IP VHI sky130_fd_pr__pfet_01v8 ad=0p pd=0u as=0p ps=0u w=1e+07u l=2e+06u
X12 VREFN VREFN VLO VLO sky130_fd_pr__nfet_01v8 ad=0p pd=0u as=0p ps=0u w=5e+06u l=2e+06u
X13 IOUT GN IN VLO sky130_fd_pr__nfet_01v8 ad=1.45e+12p pd=1.058e+07u as=0p ps=0u w=5e+06u l=150000u
X14 VLO VLO IN VLO sky130_fd_pr__nfet_01v8 ad=0p pd=0u as=0p ps=0u w=5e+06u l=2e+06u
X15 VREFP VREFP VHI VHI sky130_fd_pr__pfet_01v8 ad=0p pd=0u as=0p ps=0u w=1e+07u l=2e+06u
X16 a_314_3386# VREFN VLO VLO sky130_fd_pr__nfet_01v8 ad=0p pd=0u as=0p ps=0u w=5e+06u l=2e+06u
.ends

.subckt sky130_fd_sc_hd__inv_1 A VGND VPWR Y VNB VPB
X0 Y A VGND VNB sky130_fd_pr__nfet_01v8 ad=1.69e+11p pd=1.82e+06u as=1.69e+11p ps=1.82e+06u
+ w=650000u l=150000u
X1 Y A VPWR VPB sky130_fd_pr__pfet_01v8_hvt ad=2.6e+11p pd=2.52e+06u as=2.6e+11p ps=2.52e+06u
+ w=1e+06u l=150000u
.ends

.subckt twg_top_test IREF ULIM C50 C100 CLKIN LLIM VHI VLO VOUT OPAEN GP GN LLIM_A  ULIM_A MUX_OUT
+ UPDN ENCLK VREF_OPA RSTB GATE1 GATE2 OUT1 OUT2 B0 B1 B2 B3 B4 B5  B6 B7
Xsky130_fd_sc_hs__diode_2_1 CLKIN VLO VHI VHI VLO sky130_fd_sc_hs__diode_2
Xsky130_fd_sc_hs__diode_2_0 ULIM_A VLO VHI VHI VLO sky130_fd_sc_hs__diode_2
Xsky130_fd_sc_hs__diode_2_2 LLIM_A VLO VHI VHI VLO sky130_fd_sc_hs__diode_2
Xtwcon_0 UPDN ULIM_A LLIM_A RSTB C100 C50 MUX_OUT ENCLK GN GP CLKIN VHI VLO twcon
Xcmota_gb_rp_gp_0 cmota_gb_rp_gp_1/SBAR VREF_OPA VOUT ULIM VLO OPAEN ULIM_A VHI cmota_gb_rp_gp
Xcmota_gb_rp_gp_1 cmota_gb_rp_gp_1/SBAR VREF_OPA LLIM VOUT VLO OPAEN LLIM_A VHI cmota_gb_rp_gp
Xsky130hd_esd_0 C50 VHI VLO sky130hd_esd
Xcmota_gb_rp_gp_3 cmota_gb_rp_gp_3/SBAR VREF_OPA VOUT OUT1 VLO GATE1 OUT1 VHI cmota_gb_rp_gp
Xcmota_gb_rp_gp_2 cmota_gb_rp_gp_2/SBAR VREF_OPA VOUT OUT2 VLO GATE2 OUT2 VHI cmota_gb_rp_gp
Xsky130hd_esd_1 RSTB VHI VLO sky130hd_esd
Xsky130hd_esd_3 IREF VHI VLO sky130hd_esd
Xsky130hd_esd_2 C100 VHI VLO sky130hd_esd
Xsky130hd_esd_4 VREF_OPA VHI VLO sky130hd_esd
Xsky130hd_esd_5 OPAEN VHI VLO sky130hd_esd
Xswcap_array_1_0 B7 B6 B5 B4 B3 B2 B0 B1 VLO VOUT swcap_array_1
Xsky130hd_esd_6 CLKIN VHI VLO sky130hd_esd
Xsky130hd_esd_7 GATE1 VHI VLO sky130hd_esd
Xsky130hd_esd_9 GATE2 VHI VLO sky130hd_esd
Xisrc_0 VOUT VLO GP VHI GN IREF isrc
Xsky130_fd_sc_hd__inv_1_1 GATE2 VLO VHI cmota_gb_rp_gp_2/SBAR VLO VHI sky130_fd_sc_hd__inv_1
Xsky130_fd_sc_hd__inv_1_0 OPAEN VLO VHI cmota_gb_rp_gp_1/SBAR VLO VHI sky130_fd_sc_hd__inv_1
Xsky130_fd_sc_hd__inv_1_2 GATE1 VLO VHI cmota_gb_rp_gp_3/SBAR VLO VHI sky130_fd_sc_hd__inv_1
Xsky130hd_esd_10 VREF_OPA VHI VLO sky130hd_esd
.ends


XDUT IREF ULIM C50 C100 CLKIN LLIM VHI VLO VOUT OPAEN GP GN LLIM_A  ULIM_A MUX_OUT UPDN ENCLK
+ VREF_OPA RSTB GATE1 GATE2 OUT1 OUT2 B0 B1 B2 B3 B4 B5  B6 B7 twg_top_test


**** end user architecture code
**.ends
.end
